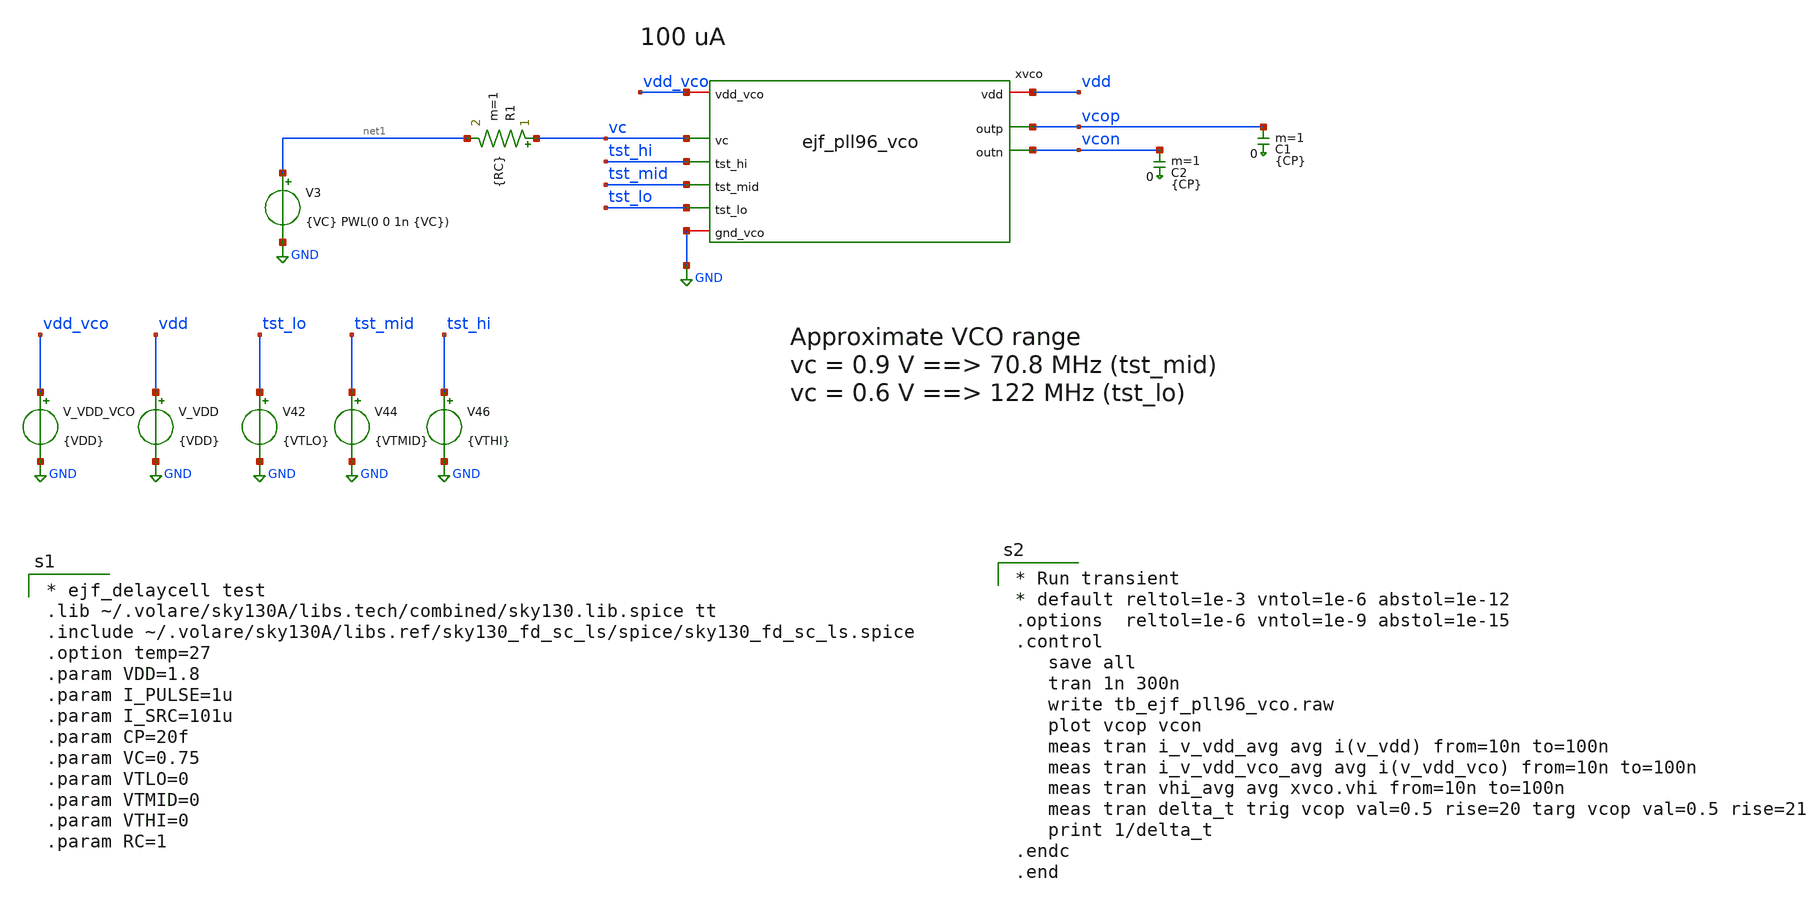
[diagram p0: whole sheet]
** sch_path: xschem/tb_ejf_pll96_vco.sch
* xschem/ejf_pll96_vco_dlycell.sym:
* Copyright (c) 2025 Eric Fogleman
**.subckt tb_ejf_pll96_vco
V_VDD vdd GND {VDD}
C1 vcop 0 {CP} m=1
C2 vcon 0 {CP} m=1
V3 net1 GND {VC} PWL(0 0 1n {VC})
xvco vdd_vco vc vdd vcop vcon GND tst_hi tst_mid tst_lo ejf_pll96_vco
V_VDD_VCO vdd_vco GND {VDD}
V42 tst_lo GND {VTLO}
V44 tst_mid GND {VTMID}
V46 tst_hi GND {VTHI}
R1 vc net1 {RC} m=1
**** begin user architecture code

* ejf_delaycell test
.lib ~/.volare/sky130A/libs.tech/combined/sky130.lib.spice tt
.include ~/.volare/sky130A/libs.ref/sky130_fd_sc_ls/spice/sky130_fd_sc_ls.spice
.option temp=27
.param VDD=1.8
.param I_PULSE=1u
.param I_SRC=101u
.param CP=20f
.param VC=0.75
.param VTLO=0
.param VTMID=0
.param VTHI=0
.param RC=1



* Run transient
* default reltol=1e-3 vntol=1e-6 abstol=1e-12
.options  reltol=1e-6 vntol=1e-9 abstol=1e-15
.control
   save all
   tran 1n 300n
   write tb_ejf_pll96_vco.raw
   plot vcop vcon
   meas tran i_v_vdd_avg avg i(v_vdd) from=10n to=100n
   meas tran i_v_vdd_vco_avg avg i(v_vdd_vco) from=10n to=100n
   meas tran vhi_avg avg xvco.vhi from=10n to=100n
   meas tran delta_t trig vcop val=0.5 rise=20 targ vcop val=0.5 rise=21
   print 1/delta_t
.endc
.end

**** end user architecture code
**.ends

* expanding   symbol:  ejf_pll96_vco.sym # of pins=9
** sym_path: xschem/ejf_pll96_vco.sym
** sch_path: xschem/ejf_pll96_vco.sch
.subckt ejf_pll96_vco vdd_vco vc vdd outp outn gnd_vco tst_hi tst_mid tst_lo
*.ipin vc
*.iopin vdd_vco
*.opin outp
*.iopin gnd_vco
*.iopin vdd
*.opin outn
*.ipin tst_mid
*.ipin tst_hi
*.ipin tst_lo
x1 vhi x1p x1n x0n x0p gnd_vco ejf_pll96_vco_dlycell
x2 vhi x2n x2p x1p x1n gnd_vco ejf_pll96_vco_dlycell
x0 vhi x0n x0p x3n x3p gnd_vco ejf_pll96_vco_dlycell
x3 vhi x3p x3n x2n x2p gnd_vco ejf_pll96_vco_dlycell
xls vdd x3p outp outn x3n gnd_vco ejf_pll96_vco_ls
XM1 vhi vc net1 vdd_vco sky130_fd_pr__pfet_01v8_lvt L=2.4 W=24 nf=4 ad='int((nf+1)/2) * W/nf * 0.29'
+ as='int((nf+2)/2) * W/nf * 0.29' pd='2*int((nf+1)/2) * (W/nf + 0.29)' ps='2*int((nf+2)/2) * (W/nf + 0.29)'
+ nrd='0.29 / W' nrs='0.29 / W' sa=0 sb=0 sd=0 mult=10 m=10
XR1 net2 vdd_vco vdd_vco sky130_fd_pr__res_high_po_2p85 L=12.1 mult=1 m=1
XR2 net1 net2 vdd_vco sky130_fd_pr__res_high_po_2p85 L=12.1 mult=1 m=1
XR3[1] vdd_vco vdd_vco vdd_vco sky130_fd_pr__res_high_po_2p85 L=12.1 mult=1 m=1
XR3[0] vdd_vco vdd_vco vdd_vco sky130_fd_pr__res_high_po_2p85 L=12.1 mult=1 m=1
XR3 net3 net6 vdd_vco sky130_fd_pr__res_high_po_0p35 L=12.1 mult=1 m=1
XR4 vc net3 vdd_vco sky130_fd_pr__res_high_po_0p35 L=12.1 mult=1 m=1
XR5 net5 net4 vdd_vco sky130_fd_pr__res_high_po_0p35 L=12.1 mult=1 m=1
XR6 net4 vc vdd_vco sky130_fd_pr__res_high_po_0p35 L=12.1 mult=1 m=1
XM2 net5 mid gnd_vco gnd sky130_fd_pr__nfet_01v8 L=0.15 W=1 nf=1 ad='int((nf+1)/2) * W/nf * 0.29' as='int((nf+2)/2) * W/nf * 0.29'
+ pd='2*int((nf+1)/2) * (W/nf + 0.29)' ps='2*int((nf+2)/2) * (W/nf + 0.29)' nrd='0.29 / W' nrs='0.29 / W'
+ sa=0 sb=0 sd=0 mult=1 m=1
XM3 net6 mid_b vdd_vco vdd sky130_fd_pr__pfet_01v8_hvt L=0.15 W=2 nf=1 ad='int((nf+1)/2) * W/nf * 0.29'
+ as='int((nf+2)/2) * W/nf * 0.29' pd='2*int((nf+1)/2) * (W/nf + 0.29)' ps='2*int((nf+2)/2) * (W/nf + 0.29)'
+ nrd='0.29 / W' nrs='0.29 / W' sa=0 sb=0 sd=0 mult=1 m=1
XM4 net3 hi_b vdd_vco vdd sky130_fd_pr__pfet_01v8_hvt L=0.15 W=2 nf=1 ad='int((nf+1)/2) * W/nf * 0.29'
+ as='int((nf+2)/2) * W/nf * 0.29' pd='2*int((nf+1)/2) * (W/nf + 0.29)' ps='2*int((nf+2)/2) * (W/nf + 0.29)'
+ nrd='0.29 / W' nrs='0.29 / W' sa=0 sb=0 sd=0 mult=1 m=1
XM5 net4 lo gnd_vco gnd sky130_fd_pr__nfet_01v8 L=0.15 W=1 nf=1 ad='int((nf+1)/2) * W/nf * 0.29' as='int((nf+2)/2) * W/nf * 0.29'
+ pd='2*int((nf+1)/2) * (W/nf + 0.29)' ps='2*int((nf+2)/2) * (W/nf + 0.29)' nrd='0.29 / W' nrs='0.29 / W'
+ sa=0 sb=0 sd=0 mult=1 m=1
x5 vdd_vco tst_lo lo lo_b gnd_vco ejf_pll96_dbuf
x6 vdd_vco tst_hi hi hi_b gnd_vco ejf_pll96_dbuf
x7 vdd_vco tst_mid mid mid_b gnd_vco ejf_pll96_dbuf
.ends


* expanding   symbol:  ejf_pll96_vco_dlycell.sym # of pins=6
** sym_path: xschem/ejf_pll96_vco_dlycell.sym
** sch_path: xschem/ejf_pll96_vco_dlycell.sch
.subckt ejf_pll96_vco_dlycell vhi outn outp inp inn gnd
*.ipin inp
*.opin outn
*.ipin inn
*.opin outp
*.iopin vhi
*.iopin gnd
XM11 outp outn gnd gnd sky130_fd_pr__nfet_01v8 L=0.44 W=1.22 nf=1 ad='int((nf+1)/2) * W/nf * 0.29' as='int((nf+2)/2) * W/nf * 0.29'
+ pd='2*int((nf+1)/2) * (W/nf + 0.29)' ps='2*int((nf+2)/2) * (W/nf + 0.29)' nrd='0.29 / W' nrs='0.29 / W'
+ sa=0 sb=0 sd=0 mult=1 m=1
XM13 outn inp gnd gnd sky130_fd_pr__nfet_01v8 L=0.44 W=4.88 nf=4 ad='int((nf+1)/2) * W/nf * 0.29' as='int((nf+2)/2) * W/nf * 0.29'
+ pd='2*int((nf+1)/2) * (W/nf + 0.29)' ps='2*int((nf+2)/2) * (W/nf + 0.29)' nrd='0.29 / W' nrs='0.29 / W'
+ sa=0 sb=0 sd=0 mult=1 m=1
XM14 outn inp vhi vhi sky130_fd_pr__pfet_01v8_hvt L=0.44 W=19.44 nf=6 ad='int((nf+1)/2) * W/nf * 0.29'
+ as='int((nf+2)/2) * W/nf * 0.29' pd='2*int((nf+1)/2) * (W/nf + 0.29)' ps='2*int((nf+2)/2) * (W/nf + 0.29)'
+ nrd='0.29 / W' nrs='0.29 / W' sa=0 sb=0 sd=0 mult=1 m=1
XM27 outn outp gnd gnd sky130_fd_pr__nfet_01v8 L=0.44 W=1.22 nf=1 ad='int((nf+1)/2) * W/nf * 0.29' as='int((nf+2)/2) * W/nf * 0.29'
+ pd='2*int((nf+1)/2) * (W/nf + 0.29)' ps='2*int((nf+2)/2) * (W/nf + 0.29)' nrd='0.29 / W' nrs='0.29 / W'
+ sa=0 sb=0 sd=0 mult=1 m=1
XM31 outp inn gnd gnd sky130_fd_pr__nfet_01v8 L=0.44 W=4.88 nf=4 ad='int((nf+1)/2) * W/nf * 0.29' as='int((nf+2)/2) * W/nf * 0.29'
+ pd='2*int((nf+1)/2) * (W/nf + 0.29)' ps='2*int((nf+2)/2) * (W/nf + 0.29)' nrd='0.29 / W' nrs='0.29 / W'
+ sa=0 sb=0 sd=0 mult=1 m=1
XM30 outp inn vhi vhi sky130_fd_pr__pfet_01v8_hvt L=0.44 W=19.44 nf=6 ad='int((nf+1)/2) * W/nf * 0.29'
+ as='int((nf+2)/2) * W/nf * 0.29' pd='2*int((nf+1)/2) * (W/nf + 0.29)' ps='2*int((nf+2)/2) * (W/nf + 0.29)'
+ nrd='0.29 / W' nrs='0.29 / W' sa=0 sb=0 sd=0 mult=1 m=1
C3 inp gnd {CP} m=1
C4 inn gnd {CP} m=1
**** begin user architecture code

* Copyright (c) Eric Fogleman 2025
* SPDX-License-Identifier: Apache-2.0

**** end user architecture code
.ends


* expanding   symbol:  ejf_pll96_vco_ls.sym # of pins=6
** sym_path: xschem/ejf_pll96_vco_ls.sym
** sch_path: xschem/ejf_pll96_vco_ls.sch
.subckt ejf_pll96_vco_ls vdd inp outp outn inn gnd
*.ipin inp
*.opin outn
*.ipin inn
*.opin outp
*.iopin vdd
*.iopin gnd
XM5 net1 ls_outn vdd vdd sky130_fd_pr__pfet_01v8_hvt L=0.15 W=2 nf=1 ad='int((nf+1)/2) * W/nf * 0.29'
+ as='int((nf+2)/2) * W/nf * 0.29' pd='2*int((nf+1)/2) * (W/nf + 0.29)' ps='2*int((nf+2)/2) * (W/nf + 0.29)'
+ nrd='0.29 / W' nrs='0.29 / W' sa=0 sb=0 sd=0 mult=1 m=1
XM1 ls_outn inp gnd gnd sky130_fd_pr__nfet_01v8 L=0.15 W=2 nf=1 ad='int((nf+1)/2) * W/nf * 0.29' as='int((nf+2)/2) * W/nf * 0.29'
+ pd='2*int((nf+1)/2) * (W/nf + 0.29)' ps='2*int((nf+2)/2) * (W/nf + 0.29)' nrd='0.29 / W' nrs='0.29 / W'
+ sa=0 sb=0 sd=0 mult=1 m=1
XM2 ls_outp inn gnd gnd sky130_fd_pr__nfet_01v8 L=0.15 W=2 nf=1 ad='int((nf+1)/2) * W/nf * 0.29' as='int((nf+2)/2) * W/nf * 0.29'
+ pd='2*int((nf+1)/2) * (W/nf + 0.29)' ps='2*int((nf+2)/2) * (W/nf + 0.29)' nrd='0.29 / W' nrs='0.29 / W'
+ sa=0 sb=0 sd=0 mult=1 m=1
XM3 net2 ls_outp vdd vdd sky130_fd_pr__pfet_01v8_hvt L=0.15 W=2 nf=1 ad='int((nf+1)/2) * W/nf * 0.29'
+ as='int((nf+2)/2) * W/nf * 0.29' pd='2*int((nf+1)/2) * (W/nf + 0.29)' ps='2*int((nf+2)/2) * (W/nf + 0.29)'
+ nrd='0.29 / W' nrs='0.29 / W' sa=0 sb=0 sd=0 mult=1 m=1
XM4 ls_outn inp net2 vdd sky130_fd_pr__pfet_01v8_hvt L=0.15 W=2 nf=1 ad='int((nf+1)/2) * W/nf * 0.29'
+ as='int((nf+2)/2) * W/nf * 0.29' pd='2*int((nf+1)/2) * (W/nf + 0.29)' ps='2*int((nf+2)/2) * (W/nf + 0.29)'
+ nrd='0.29 / W' nrs='0.29 / W' sa=0 sb=0 sd=0 mult=1 m=1
XM6 ls_outp inn net1 vdd sky130_fd_pr__pfet_01v8_hvt L=0.15 W=2 nf=1 ad='int((nf+1)/2) * W/nf * 0.29'
+ as='int((nf+2)/2) * W/nf * 0.29' pd='2*int((nf+1)/2) * (W/nf + 0.29)' ps='2*int((nf+2)/2) * (W/nf + 0.29)'
+ nrd='0.29 / W' nrs='0.29 / W' sa=0 sb=0 sd=0 mult=1 m=1
XM7 outn ls_outp gnd gnd sky130_fd_pr__nfet_01v8 L=0.15 W=2 nf=1 ad='int((nf+1)/2) * W/nf * 0.29' as='int((nf+2)/2) * W/nf * 0.29'
+ pd='2*int((nf+1)/2) * (W/nf + 0.29)' ps='2*int((nf+2)/2) * (W/nf + 0.29)' nrd='0.29 / W' nrs='0.29 / W'
+ sa=0 sb=0 sd=0 mult=1 m=1
XM8 outn ls_outp vdd vdd sky130_fd_pr__pfet_01v8_hvt L=0.15 W=4 nf=1 ad='int((nf+1)/2) * W/nf * 0.29'
+ as='int((nf+2)/2) * W/nf * 0.29' pd='2*int((nf+1)/2) * (W/nf + 0.29)' ps='2*int((nf+2)/2) * (W/nf + 0.29)'
+ nrd='0.29 / W' nrs='0.29 / W' sa=0 sb=0 sd=0 mult=1 m=1
XM9 outp ls_outn gnd gnd sky130_fd_pr__nfet_01v8 L=0.15 W=2 nf=1 ad='int((nf+1)/2) * W/nf * 0.29' as='int((nf+2)/2) * W/nf * 0.29'
+ pd='2*int((nf+1)/2) * (W/nf + 0.29)' ps='2*int((nf+2)/2) * (W/nf + 0.29)' nrd='0.29 / W' nrs='0.29 / W'
+ sa=0 sb=0 sd=0 mult=1 m=1
XM10 outp ls_outn vdd vdd sky130_fd_pr__pfet_01v8_hvt L=0.15 W=4 nf=1 ad='int((nf+1)/2) * W/nf * 0.29'
+ as='int((nf+2)/2) * W/nf * 0.29' pd='2*int((nf+1)/2) * (W/nf + 0.29)' ps='2*int((nf+2)/2) * (W/nf + 0.29)'
+ nrd='0.29 / W' nrs='0.29 / W' sa=0 sb=0 sd=0 mult=1 m=1
.ends


* expanding   symbol:  ejf_pll96_dbuf.sym # of pins=5
** sym_path: xschem/ejf_pll96_dbuf.sym
** sch_path: xschem/ejf_pll96_dbuf.sch
.subckt ejf_pll96_dbuf vdd a y y_b gnd
*.ipin a
*.iopin vdd
*.iopin gnd
*.opin y
*.opin y_b
XMP1 y_b a vdd vdd sky130_fd_pr__pfet_01v8_hvt L=0.15 W=2 nf=1 ad='int((nf+1)/2) * W/nf * 0.29' as='int((nf+2)/2) * W/nf * 0.29'
+ pd='2*int((nf+1)/2) * (W/nf + 0.29)' ps='2*int((nf+2)/2) * (W/nf + 0.29)' nrd='0.29 / W' nrs='0.29 / W'
+ sa=0 sb=0 sd=0 mult=1 m=1
XMP3 y y_b vdd vdd sky130_fd_pr__pfet_01v8_hvt L=0.15 W=2 nf=1 ad='int((nf+1)/2) * W/nf * 0.29' as='int((nf+2)/2) * W/nf * 0.29'
+ pd='2*int((nf+1)/2) * (W/nf + 0.29)' ps='2*int((nf+2)/2) * (W/nf + 0.29)' nrd='0.29 / W' nrs='0.29 / W'
+ sa=0 sb=0 sd=0 mult=1 m=1
XMN4 y y_b gnd gnd sky130_fd_pr__nfet_01v8 L=0.15 W=1 nf=1 ad='int((nf+1)/2) * W/nf * 0.29' as='int((nf+2)/2) * W/nf * 0.29'
+ pd='2*int((nf+1)/2) * (W/nf + 0.29)' ps='2*int((nf+2)/2) * (W/nf + 0.29)' nrd='0.29 / W' nrs='0.29 / W'
+ sa=0 sb=0 sd=0 mult=1 m=1
XMN2 y_b a gnd gnd sky130_fd_pr__nfet_01v8 L=0.15 W=1 nf=1 ad='int((nf+1)/2) * W/nf * 0.29' as='int((nf+2)/2) * W/nf * 0.29'
+ pd='2*int((nf+1)/2) * (W/nf + 0.29)' ps='2*int((nf+2)/2) * (W/nf + 0.29)' nrd='0.29 / W' nrs='0.29 / W'
+ sa=0 sb=0 sd=0 mult=1 m=1
.ends

.GLOBAL GND
.end
